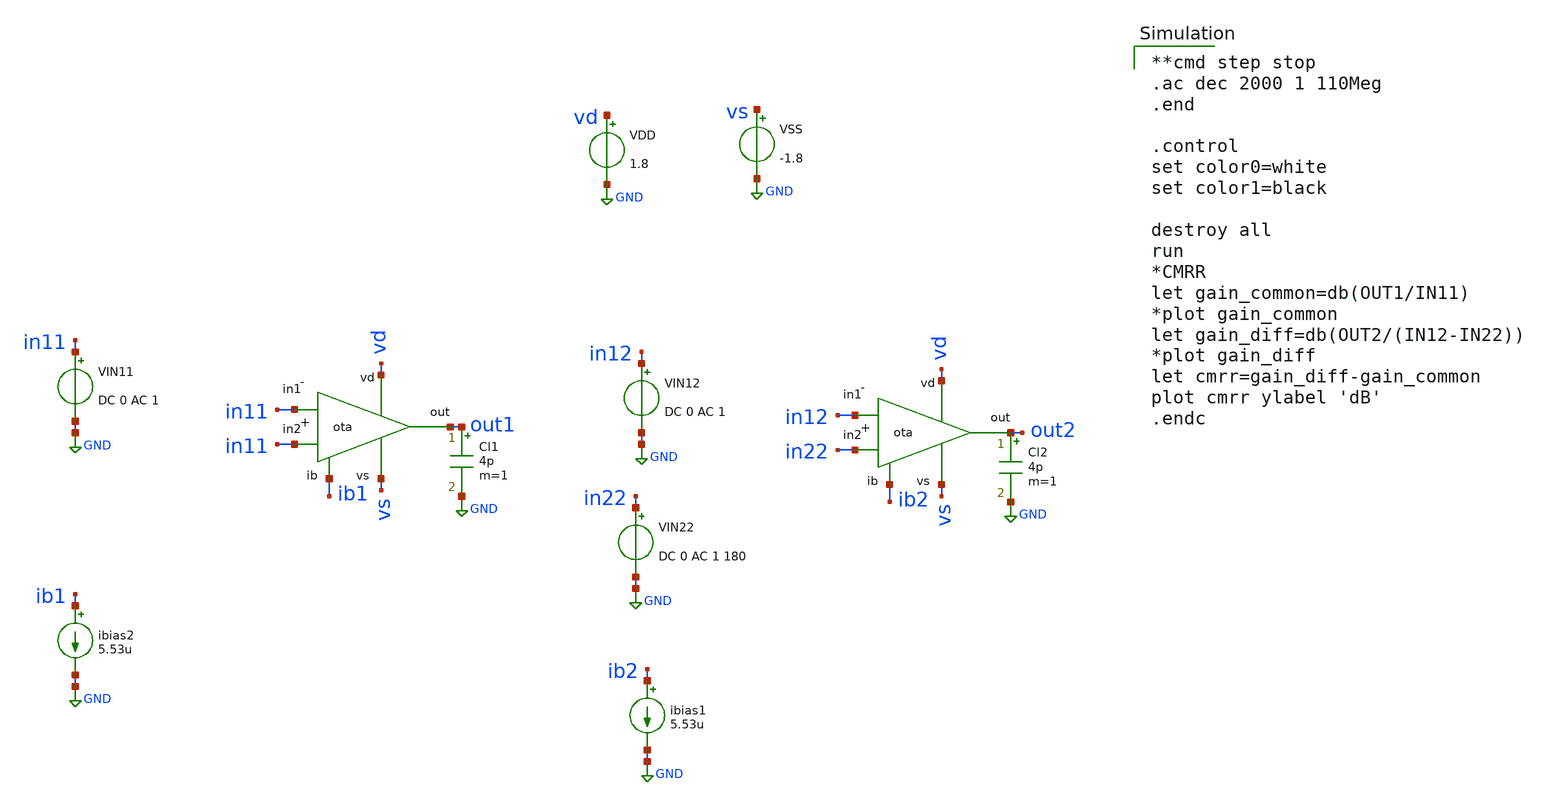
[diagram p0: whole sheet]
** sch_path: amp-op/xschem/ota_tb-CMRR.sch
* Copyright 2020 Stefan Frederik Schippers
* Licensed under the Apache License, Version 2.0 (the "License");
* you may not use this file except in compliance with the License.
* You may obtain a copy of the License at
* https://www.apache.org/licenses/LICENSE-2.0
* Unless required by applicable law or agreed to in writing, software
* distributed under the License is distributed on an "AS IS" BASIS,
* WITHOUT WARRANTIES OR CONDITIONS OF ANY KIND, either express or implied.
* See the License for the specific language governing permissions and
* limitations under the License.
**.subckt ota_tb-CMRR
VIN11 in11 GND DC 0 AC 1
ibias2 ib1 GND 5.53u
VDD vd GND 1.8
VSS vs GND -1.8
VIN12 in12 GND DC 0 AC 1
ibias1 ib2 GND 5.53u
VIN22 in22 GND DC 0 AC 1 180
Cl1 out1 GND 4p m=1
Cl2 out2 GND 4p m=1
X1 vd ib1 out1 in11 in11 vs ota
X2 vd ib2 out2 in22 in12 vs ota
**** begin user architecture code

**cmd step stop
.ac dec 2000 1 110Meg
.end

.control
set color0=white
set color1=black

destroy all
run
*CMRR
let gain_common=db(OUT1/IN11)
*plot gain_common
let gain_diff=db(OUT2/(IN12-IN22))
*plot gain_diff
let cmrr=gain_diff-gain_common
plot cmrr ylabel 'dB'
.endc


.lib /home/hugodg/sky130_workspace/skywater-pdk/libraries/sky130_fd_pr_ngspice/latest/models/sky130.lib.spice tt

**** end user architecture code
**.ends

* expanding   symbol:  /home/hugodg/projects-sky130/temp-sensor/amp-op/xschem/ota.sym # of pins=6
** sym_path: amp-op/xschem/ota.sym
** sch_path: amp-op/xschem/ota.sch
.subckt ota vd ib out in2 in1 vs
*.iopin vd
*.iopin vs
*.iopin ib
*.ipin in1
*.ipin in2
*.opin out
XCC e d sky130_fd_pr__cap_mim_m3_1 W=21 L=21 MF=1 m=1
XM5 ib ib vd vd sky130_fd_pr__pfet_g5v0d10v5 L=1 W=6 nf=1 ad='int((nf+1)/2) * W/nf * 0.29' as='int((nf+2)/2) * W/nf * 0.29'
+ pd='2*int((nf+1)/2) * (W/nf + 0.29)' ps='2*int((nf+2)/2) * (W/nf + 0.29)' nrd='0.29 / W' nrs='0.29 / W'
+ sa=0 sb=0 sd=0 mult=1 m=1
XM6 b ib vd vd sky130_fd_pr__pfet_g5v0d10v5 L=1 W=6 nf=1 ad='int((nf+1)/2) * W/nf * 0.29' as='int((nf+2)/2) * W/nf * 0.29'
+ pd='2*int((nf+1)/2) * (W/nf + 0.29)' ps='2*int((nf+2)/2) * (W/nf + 0.29)' nrd='0.29 / W' nrs='0.29 / W'
+ sa=0 sb=0 sd=0 mult=1 m=1
XM8 e ib vd vd sky130_fd_pr__pfet_g5v0d10v5 L=1 W=30 nf=4 ad='int((nf+1)/2) * W/nf * 0.29' as='int((nf+2)/2) * W/nf * 0.29'
+ pd='2*int((nf+1)/2) * (W/nf + 0.29)' ps='2*int((nf+2)/2) * (W/nf + 0.29)' nrd='0.29 / W' nrs='0.29 / W'
+ sa=0 sb=0 sd=0 mult=1 m=1
XM10 out ib vd vd sky130_fd_pr__pfet_g5v0d10v5 L=1 W=6 nf=1 ad='int((nf+1)/2) * W/nf * 0.29' as='int((nf+2)/2) * W/nf * 0.29'
+ pd='2*int((nf+1)/2) * (W/nf + 0.29)' ps='2*int((nf+2)/2) * (W/nf + 0.29)' nrd='0.29 / W' nrs='0.29 / W'
+ sa=0 sb=0 sd=0 mult=1 m=1
XM9 vs e out out sky130_fd_pr__pfet_g5v0d10v5 L=1 W=6 nf=1 ad='int((nf+1)/2) * W/nf * 0.29' as='int((nf+2)/2) * W/nf * 0.29'
+ pd='2*int((nf+1)/2) * (W/nf + 0.29)' ps='2*int((nf+2)/2) * (W/nf + 0.29)' nrd='0.29 / W' nrs='0.29 / W'
+ sa=0 sb=0 sd=0 mult=1 m=1
XM1 c in1 b b sky130_fd_pr__pfet_g5v0d10v5 L=1 W=3 nf=1 ad='int((nf+1)/2) * W/nf * 0.29' as='int((nf+2)/2) * W/nf * 0.29'
+ pd='2*int((nf+1)/2) * (W/nf + 0.29)' ps='2*int((nf+2)/2) * (W/nf + 0.29)' nrd='0.29 / W' nrs='0.29 / W'
+ sa=0 sb=0 sd=0 mult=1 m=1
XM2 d in2 b b sky130_fd_pr__pfet_g5v0d10v5 L=1 W=3 nf=1 ad='int((nf+1)/2) * W/nf * 0.29' as='int((nf+2)/2) * W/nf * 0.29'
+ pd='2*int((nf+1)/2) * (W/nf + 0.29)' ps='2*int((nf+2)/2) * (W/nf + 0.29)' nrd='0.29 / W' nrs='0.29 / W'
+ sa=0 sb=0 sd=0 mult=1 m=1
XM3 c c vs vs sky130_fd_pr__nfet_g5v0d10v5 L=1 W=1 nf=1 ad='int((nf+1)/2) * W/nf * 0.29' as='int((nf+2)/2) * W/nf * 0.29'
+ pd='2*int((nf+1)/2) * (W/nf + 0.29)' ps='2*int((nf+2)/2) * (W/nf + 0.29)' nrd='0.29 / W' nrs='0.29 / W'
+ sa=0 sb=0 sd=0 mult=1 m=1
XM4 d c vs vs sky130_fd_pr__nfet_g5v0d10v5 L=1 W=1 nf=1 ad='int((nf+1)/2) * W/nf * 0.29' as='int((nf+2)/2) * W/nf * 0.29'
+ pd='2*int((nf+1)/2) * (W/nf + 0.29)' ps='2*int((nf+2)/2) * (W/nf + 0.29)' nrd='0.29 / W' nrs='0.29 / W'
+ sa=0 sb=0 sd=0 mult=1 m=1
XM7 e d vs vs sky130_fd_pr__nfet_g5v0d10v5 L=1 W=9 nf=2 ad='int((nf+1)/2) * W/nf * 0.29' as='int((nf+2)/2) * W/nf * 0.29'
+ pd='2*int((nf+1)/2) * (W/nf + 0.29)' ps='2*int((nf+2)/2) * (W/nf + 0.29)' nrd='0.29 / W' nrs='0.29 / W'
+ sa=0 sb=0 sd=0 mult=1 m=1
**** begin user architecture code


RR0 vs.n20 vs.n14 202.916
R1 vs.n7 vs.n1 202.916
R2 vs.n21 vs.n20 121.975
R3 vs.n8 vs.n7 121.975
R4 vs.n28 vs.n27 2.673
R5 vs.n29 vs.n28 1.458
R6 vs vs.n29 1.104
R7 vs.n27 vs.n26 0.911
R8 vs.n25 vs.n24 0.348
R9 vs.n12 vs.n11 0.348
R10 vs.n28 vs.n25 0.135
R11 vs.n29 vs.n12 0.135
R12 vs.n25 vs.n21 0.09
R13 vs.n12 vs.n8 0.09
R14 vs.n14 vs.n13 0.04
R15 vs.n1 vs.n0 0.04
R16 vs.n18 vs.n17 0.037
R17 vs.n5 vs.n4 0.037
R18 vs.n16 vs.n15 0.034
R19 vs.n20 vs.n19 0.034
R20 vs.n3 vs.n2 0.034
R21 vs.n7 vs.n6 0.034
R22 vs.n17 vs.n16 0.016
R23 vs.n4 vs.n3 0.016
R24 vs.n19 vs.n18 0.016
R25 vs.n6 vs.n5 0.016
R26 vs.n24 vs.n23 0.001
R27 vs.n11 vs.n10 0.001
R28 vs.n23 vs.n22 0.001
R29 vs.n10 vs.n9 0.001
R30 out.n10 out.n4 394.54
R31 out.n11 out.n10 313.599
R32 out.n12 out.n2 0.386
R33 out out.n12 0.168
R34 out.n12 out.n11 0.052
R35 out.n4 out.n3 0.013
R36 out.n8 out.n7 0.003
R37 out.n6 out.n5 0.003
R38 out.n10 out.n9 0.003
R39 out.n7 out.n6 0.002
R40 out.n9 out.n8 0.002
R41 out.n2 out.n1 0.001
R42 out.n1 out.n0 0.001
R43 in1 in1.t0 88.743
R44 in2 in2.t0 90.145
R45 ib.n3 ib.t5 196.178
R46 ib.n2 ib.t3 196.178
R47 ib.n1 ib.t4 196.178
R48 ib.n0 ib.t6 196.178
R49 ib.n0 ib.t7 162.082
R50 ib.n5 ib.t0 160.028
R51 ib.n4 ib.t2 160.028
R52 ib.n6 ib.t1 6.282
R53 ib.n4 ib.n3 2.041
R54 ib.n5 ib.n4 2.041
R55 ib ib.n6 1.518
R56 ib.n1 ib.n0 0.537
R57 ib.n2 ib.n1 0.537
R58 ib.n3 ib.n2 0.537
R59 ib.n6 ib.n5 0.266
R60 vd.n5 vd.n1 507.374
R61 vd.n32 vd.n26 394.54
R62 vd.n19 vd.n13 394.54
R63 vd.n44 vd.n43 394.54
R64 vd.n7 vd.n6 331.818
R65 vd.n33 vd.n32 313.599
R66 vd.n20 vd.n19 313.599
R67 vd.n45 vd.n44 313.599
R68 vd vd.n49 3.951
R69 vd.n35 vd.n34 2.876
R70 vd.n8 vd.n7 1.417
R71 vd.n36 vd.n35 1.333
R72 vd.n35 vd.n21 0.835
R73 vd.n34 vd.n24 0.386
R74 vd.n21 vd.n11 0.386
R75 vd.n49 vd.n48 0.376
R76 vd vd.n36 0.229
R77 vd.n36 vd.n8 0.211
R78 vd.n49 vd.n45 0.063
R79 vd.n34 vd.n33 0.052
R80 vd.n21 vd.n20 0.052
R81 vd.n26 vd.n25 0.013
R82 vd.n13 vd.n12 0.013
R83 vd.n43 vd.n42 0.013
R84 vd.n6 vd.n5 0.004
R85 vd.n1 vd.n0 0.004
R86 vd.n30 vd.n29 0.003
R87 vd.n17 vd.n16 0.003
R88 vd.n40 vd.n39 0.003
R89 vd.n28 vd.n27 0.003
R90 vd.n32 vd.n31 0.003
R91 vd.n15 vd.n14 0.003
R92 vd.n19 vd.n18 0.003
R93 vd.n44 vd.n41 0.003
R94 vd.n38 vd.n37 0.003
R95 vd.n29 vd.n28 0.002
R96 vd.n16 vd.n15 0.002
R97 vd.n41 vd.n40 0.002
R98 vd.n31 vd.n30 0.002
R99 vd.n18 vd.n17 0.002
R100 vd.n39 vd.n38 0.002
R101 vd.n4 vd.n3 0.002
R102 vd.n3 vd.n2 0.002
R103 vd.n5 vd.n4 0.002
R104 vd.n48 vd.n47 0.001
R105 vd.n24 vd.n23 0.001
R106 vd.n11 vd.n10 0.001
R107 vd.n23 vd.n22 0.001
R108 vd.n10 vd.n9 0.001
R109 vd.n47 vd.n46 0.001
C0 w_460_9160# vs 0.25fF
C1 vs out 0.29fF
C2 vs e 0.43fF
C3 in2 in1 0.06fF
C4 w_460_9160# vd 0.57fF
C5 in2 d 0.06fF
C6 vd out 0.34fF
C7 vs c 0.57fF
C8 w_460_9160# ib 0.42fF
C9 ib out 0.09fF
C10 vd e 1.05fF
C11 ib e 0.91fF
C12 vd c 0.00fF
C13 ib c 0.01fF
C14 vs vd 0.07fF
C15 w_460_9160# in1 0.18fF
C16 vs ib 0.06fF
C17 w_460_9160# d 0.31fF
C18 out d 0.01fF
C19 e d 0.26fF
C20 ib vd 2.28fF
C21 in1 c 0.25fF
C22 c d 0.13fF
C23 in1 vs 0.08fF
C24 in2 w_460_9160# 0.53fF
C25 vs d 0.55fF
C26 in1 vd 0.01fF
C27 vd d 0.01fF
C28 in1 ib 0.03fF
C29 in2 c 0.07fF
C30 ib d 0.04fF
C31 in2 vs 0.05fF
C32 w_460_9160# e 0.07fF
C33 in2 vd 0.02fF
C34 e out 0.05fF
C35 in2 ib 0.20fF
C36 in1 d 0.01fF
C37 w_460_9160# c 0.56fF
C38 c e 0.00fF
C39 w_460_9160# 0 7.23fF
C40 vd.n0 0 0.19fF $ **FLOATING
C41 vd.n1 0 3.35fF $ **FLOATING
C42 vd.n2 0 0.16fF $ **FLOATING
C43 vd.n3 0 0.33fF $ **FLOATING
C44 vd.n4 0 2.51fF $ **FLOATING
C45 vd.n5 0 2.68fF $ **FLOATING
C46 vd.n6 0 0.32fF $ **FLOATING
C47 vd.n7 0 3.66fF $ **FLOATING
C48 vd.n8 0 2.18fF $ **FLOATING
C49 vd.n9 0 1.48fF $ **FLOATING
C50 vd.n10 0 0.03fF $ **FLOATING
C51 vd.n11 0 0.12fF $ **FLOATING
C52 vd.n12 0 1.48fF $ **FLOATING
C53 vd.n13 0 0.13fF $ **FLOATING
C54 vd.n14 0 0.11fF $ **FLOATING
C55 vd.n15 0 0.22fF $ **FLOATING
C56 vd.n16 0 1.02fF $ **FLOATING
C57 vd.n17 0 1.02fF $ **FLOATING
C58 vd.n18 0 0.22fF $ **FLOATING
C59 vd.n19 0 0.11fF $ **FLOATING
C60 vd.n20 0 0.07fF $ **FLOATING
C61 vd.n21 0 0.70fF $ **FLOATING
C62 vd.n22 0 1.48fF $ **FLOATING
C63 vd.n23 0 0.03fF $ **FLOATING
C64 vd.n24 0 0.12fF $ **FLOATING
C65 vd.n25 0 1.48fF $ **FLOATING
C66 vd.n26 0 0.13fF $ **FLOATING
C67 vd.n27 0 0.11fF $ **FLOATING
C68 vd.n28 0 0.22fF $ **FLOATING
C69 vd.n29 0 1.02fF $ **FLOATING
C70 vd.n30 0 1.02fF $ **FLOATING
C71 vd.n31 0 0.22fF $ **FLOATING
C72 vd.n32 0 0.11fF $ **FLOATING
C73 vd.n33 0 0.07fF $ **FLOATING
C74 vd.n34 0 0.81fF $ **FLOATING
C75 vd.n35 0 0.26fF $ **FLOATING
C76 vd.n36 0 0.10fF $ **FLOATING
C77 vd.n37 0 0.11fF $ **FLOATING
C78 vd.n38 0 0.22fF $ **FLOATING
C79 vd.n39 0 1.02fF $ **FLOATING
C80 vd.n40 0 1.02fF $ **FLOATING
C81 vd.n41 0 0.22fF $ **FLOATING
C82 vd.n42 0 1.48fF $ **FLOATING
C83 vd.n43 0 0.13fF $ **FLOATING
C84 vd.n44 0 0.11fF $ **FLOATING
C85 vd.n45 0 0.07fF $ **FLOATING
C86 vd.n46 0 1.48fF $ **FLOATING
C87 vd.n47 0 0.03fF $ **FLOATING
C88 vd.n48 0 0.12fF $ **FLOATING
C89 vd.n49 0 0.87fF $ **FLOATING
C90 ib.t1 0 0.12fF
C91 ib.t7 0 0.52fF
C92 ib.t6 0 0.62fF
C93 ib.n0 0 0.57fF $ **FLOATING
C94 ib.t4 0 0.62fF
C95 ib.n1 0 0.26fF $ **FLOATING
C96 ib.t3 0 0.62fF
C97 ib.n2 0 0.26fF $ **FLOATING
C98 ib.t5 0 0.62fF
C99 ib.n3 0 0.31fF $ **FLOATING
C100 ib.t2 0 0.52fF
C101 ib.n4 0 0.32fF $ **FLOATING
C102 ib.t0 0 0.52fF
C103 ib.n5 0 0.26fF $ **FLOATING
C104 ib.n6 0 0.34fF $ **FLOATING
C105 out.n0 0 0.93fF $ **FLOATING
C106 out.n1 0 0.02fF $ **FLOATING
C107 out.n2 0 0.07fF $ **FLOATING
C108 out.n3 0 0.93fF $ **FLOATING
C109 out.n4 0 0.08fF $ **FLOATING
C110 out.n5 0 0.07fF $ **FLOATING
C111 out.n6 0 0.14fF $ **FLOATING
C112 out.n7 0 0.64fF $ **FLOATING
C113 out.n8 0 0.64fF $ **FLOATING
C114 out.n9 0 0.14fF $ **FLOATING
C115 out.n10 0 0.07fF $ **FLOATING
C116 out.n11 0 0.04fF $ **FLOATING
C117 out.n12 0 0.42fF $ **FLOATING
C118 vs.n0 0 0.94fF $ **FLOATING
C119 vs.n1 0 0.10fF $ **FLOATING
C120 vs.n2 0 0.08fF $ **FLOATING
C121 vs.n3 0 0.18fF $ **FLOATING
C122 vs.n4 0 0.53fF $ **FLOATING
C123 vs.n5 0 0.53fF $ **FLOATING
C124 vs.n6 0 0.18fF $ **FLOATING
C125 vs.n7 0 0.08fF $ **FLOATING
C126 vs.n8 0 0.06fF $ **FLOATING
C127 vs.n9 0 0.94fF $ **FLOATING
C128 vs.n10 0 0.04fF $ **FLOATING
C129 vs.n11 0 0.13fF $ **FLOATING
C130 vs.n12 0 0.29fF $ **FLOATING
C131 vs.n13 0 0.94fF $ **FLOATING
C132 vs.n14 0 0.10fF $ **FLOATING
C133 vs.n15 0 0.08fF $ **FLOATING
C134 vs.n16 0 0.18fF $ **FLOATING
C135 vs.n17 0 0.53fF $ **FLOATING
C136 vs.n18 0 0.53fF $ **FLOATING
C137 vs.n19 0 0.18fF $ **FLOATING
C138 vs.n20 0 0.08fF $ **FLOATING
C139 vs.n21 0 0.06fF $ **FLOATING
C140 vs.n22 0 0.94fF $ **FLOATING
C141 vs.n23 0 0.04fF $ **FLOATING
C142 vs.n24 0 0.13fF $ **FLOATING
C143 vs.n25 0 0.29fF $ **FLOATING
C144 vs.n26 0 9.30fF $ **FLOATING
C145 vs.n27 0 2.86fF $ **FLOATING
C146 vs.n28 0 0.47fF $ **FLOATING
C147 vs.n29 0 0.23fF $ **FLOATING
C148 vd 0 27.83fF
C149 ib 0 -31.45fF
C150 vs 0 21.62fF
C151 c 0 -2.70fF
C152 in2 0 0.40fF
C153 in1 0 1.82fF
C154 out 0 5.47fF
C155 e 0 2.80fF
C156 d 0 16.90fF


**** end user architecture code
.ends

.GLOBAL GND
.end
